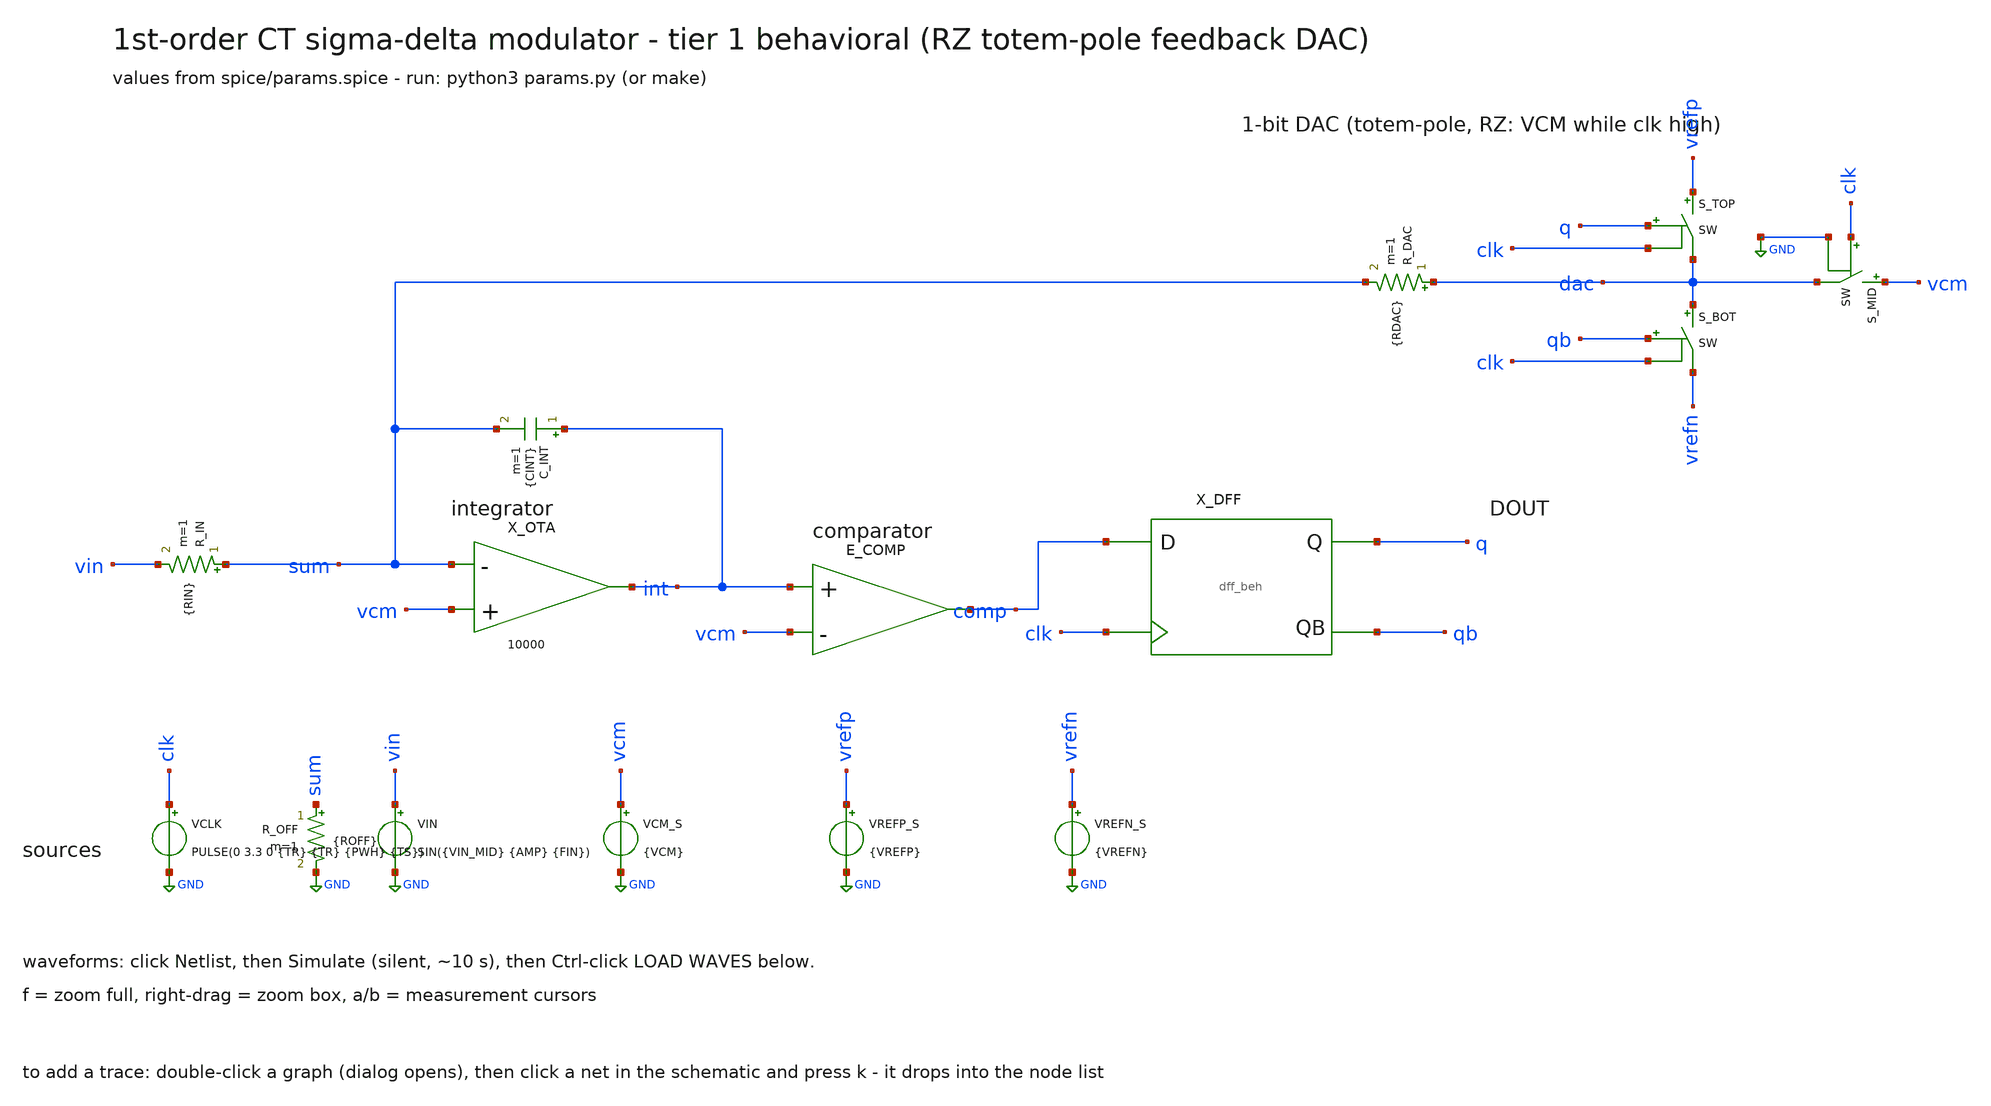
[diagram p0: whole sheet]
** sch_path: xschem/tier1_sdm.sch
**.subckt tier1_sdm
R_IN sum vin {RIN} m=1
X_OTA int GND vcm sum 10000
C_INT int sum {CINT} m=1
E_COMP comp GND VOL='1.65+1.65*tanh(2000*(v( int )-v( vcm )))'
X_DFF comp clk q qb dff_beh
S_TOP vrefp dac q clk SW
S_BOT dac vrefn qb clk SW
S_MID vcm dac clk GND SW
R_DAC dac sum {RDAC} m=1
VCLK clk GND PULSE(0 3.3 0 {TR} {TR} {PWH} {TS})
VIN vin GND SIN({VIN_MID} {AMP} {FIN})
VCM_S vcm GND {VCM}
VREFP_S vrefp GND {VREFP}
VREFN_S vrefn GND {VREFN}
R_OFF sum GND {ROFF} m=1
**** begin user architecture code

.include params.spice
.model SW sw vt=1.65 vh=0.1 ron=100 roff=1e9
* behavioral OTA: single-pole, slew-limited (AOL, GBW [Hz], SR [V/s])
.subckt ota_beh PLUS MINUS OUT AOL=10000 GBW=200e6 SR=2e8 FP2=100e9
.param CI=100f
.param GMI={6.2831853*GBW*CI}
.param ILIM={SR*CI}
.param RO={AOL/GMI}
.param RP2=1k
.param CP2={1/(6.2831853*RP2*FP2)}
B_GM 0 x I={ILIM}*tanh({GMI}*(v(PLUS)-v(MINUS))/{ILIM})
R_O x 0 {RO}
C_O x 0 {CI}
* second (parasitic) pole at FP2, buffered so it never loads the
* integrator node -- excess-phase knob for the PM requirement sweep
E_INT xb 0 x 0 1
R_P2 xb y {RP2}
C_P2 y 0 {CP2}
E_BUF OUT 0 y 0 1
.ends
* behavioral DFF: master/slave sample-and-hold of D at rising CLK edge
.subckt dff_beh D CLK Q QB
V_L vddl 0 3.3
S_M D m vddl CLK SW
C_M m 0 100f
S_S m qraw CLK 0 SW
C_Q qraw 0 100f
E_Q Q 0 VOL='1.65+1.65*tanh(20*(v(qraw)-1.65))'
E_QB QB 0 VOL='3.3-v(Q)'
.ends
.ic v(int)={VCM}
* gear integration: the OTA model's parasitic second pole (FP2) is a fast
* state; default trapezoidal rings on it at TSTEP and the ringing reads as
* ~2/8 dB of fake SNDR loss (fast/precision). Gear is L-stable and damps it.
.options method=gear
.tran {TSTEP} {TSTOP} uic
.control
run
write tier1_sdm.raw
wrdata tier1_out.csv v(q) v(clk) v(vin) v(int) v(dac) v(comp)
.endc


**** end user architecture code
**.ends
.GLOBAL GND
.end
